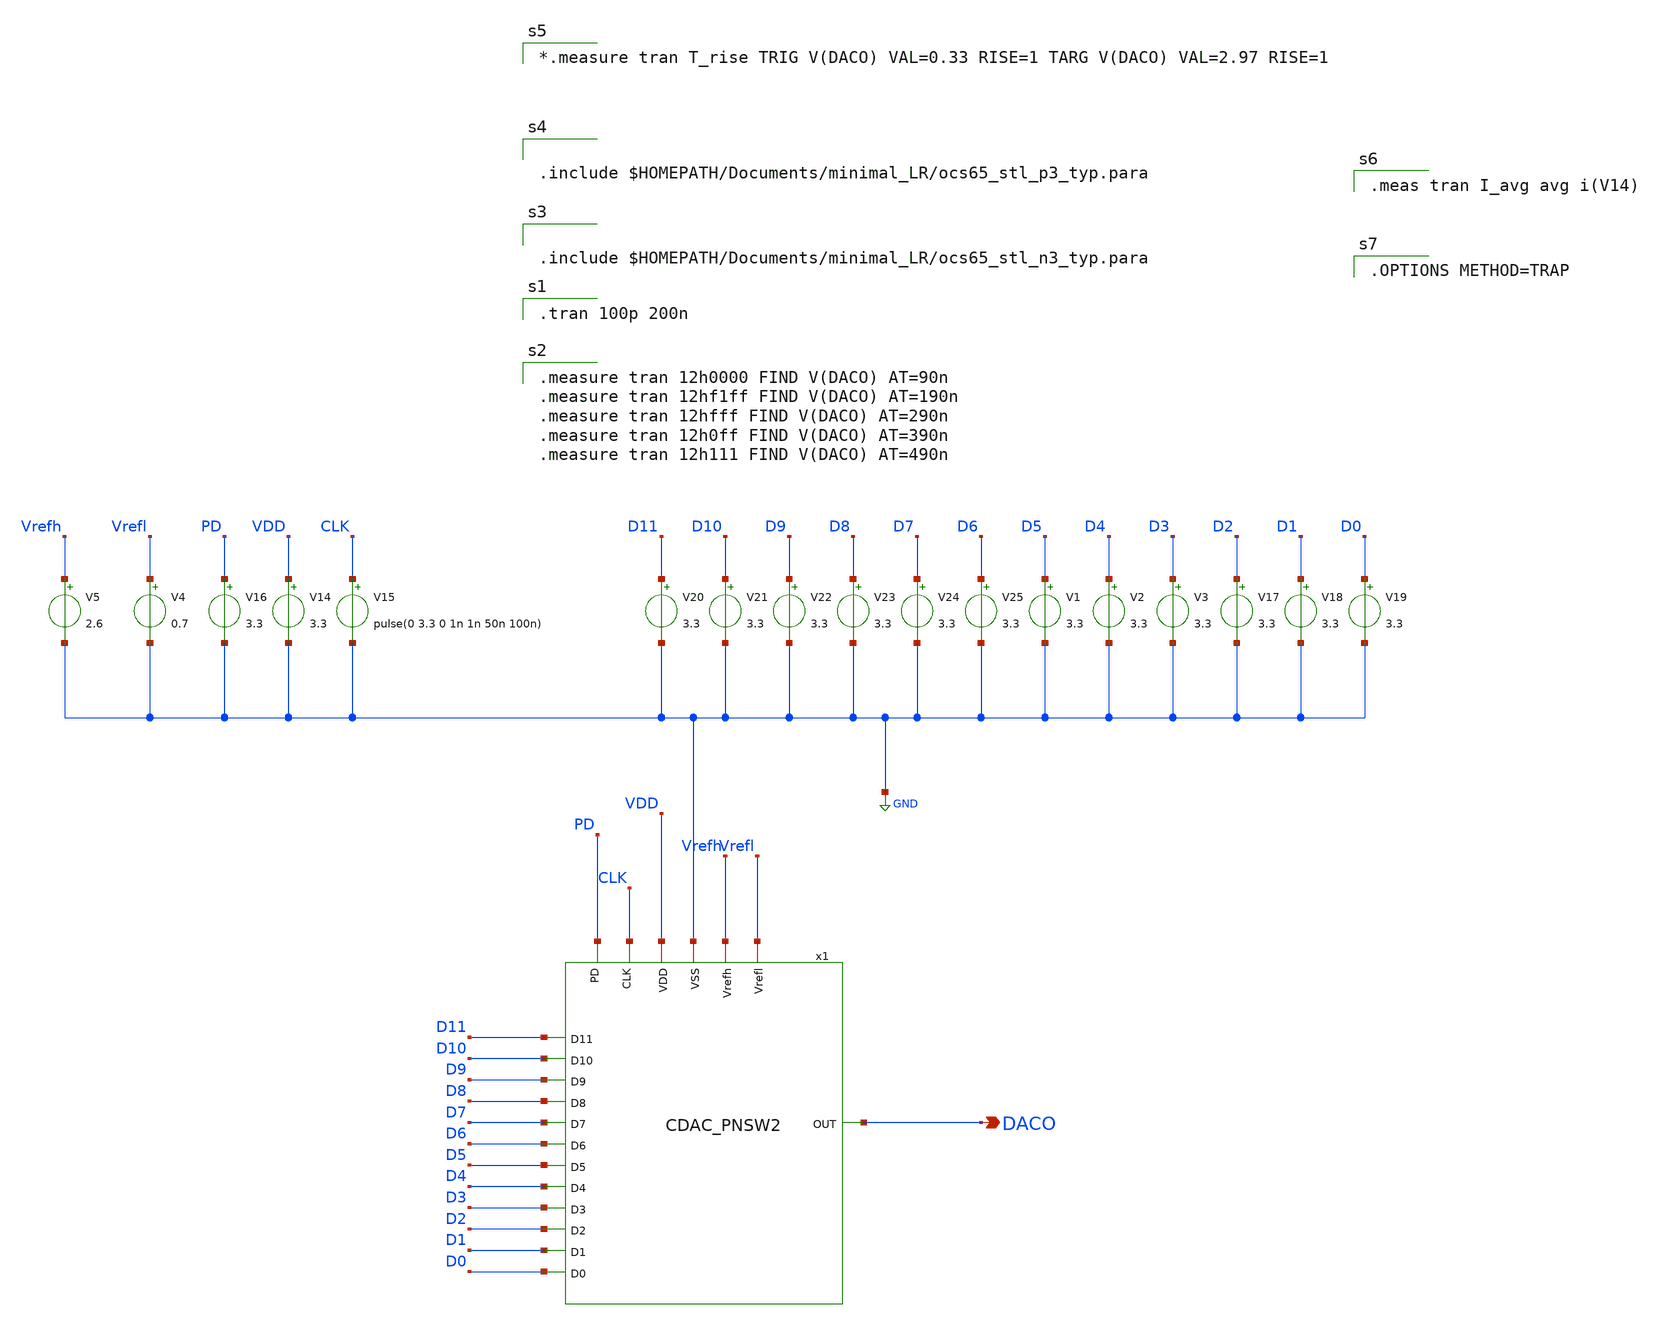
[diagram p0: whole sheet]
** sch_path: CDAC_sim.sch
**.subckt CDAC_sim DACO
*.opin DACO
V14 VDD GND 3.3
V15 CLK GND pulse(0 3.3 0 1n 1n 50n 100n)
V16 PD GND 3.3
V1 D5 GND 3.3
V2 D4 GND 3.3
V3 D3 GND 3.3
V17 D2 GND 3.3
V18 D1 GND 3.3
V19 D0 GND 3.3
V20 D11 GND 3.3
V21 D10 GND 3.3
V22 D9 GND 3.3
V23 D8 GND 3.3
V24 D7 GND 3.3
V25 D6 GND 3.3
V4 Vrefl GND 0.7
V5 Vrefh GND 2.6
x1 CLK D11 D7 D10 D1 D0 D9 D8 D2 D6 D5 D4 D3 DACO GND VDD Vrefl Vrefh PD CDAC_PNSW2
**** begin user architecture code

.tran 100p 200n


.measure tran 12h0000 FIND V(DACO) AT=90n
.measure tran 12hf1ff FIND V(DACO) AT=190n
.measure tran 12hfff FIND V(DACO) AT=290n
.measure tran 12h0ff FIND V(DACO) AT=390n
.measure tran 12h111 FIND V(DACO) AT=490n



.include $HOMEPATH/Documents/minimal_LR/ocs65_stl_n3_typ.para



.include $HOMEPATH/Documents/minimal_LR/ocs65_stl_p3_typ.para


*.measure tran T_rise TRIG V(DACO) VAL=0.33 RISE=1 TARG V(DACO) VAL=2.97 RISE=1


.meas tran I_avg avg i(V14)


.OPTIONS METHOD=TRAP

**** end user architecture code
**.ends

* expanding   symbol:  CDAC_PNSW2.sym # of pins=19
** sym_path: CDAC_PNSW2.sym
** sch_path: CDAC_PNSW2.sch
.subckt CDAC_PNSW2 CLK D11 D7 D10 D1 D0 D9 D8 D2 D6 D5 D4 D3 OUT VSS VDD Vrefl Vrefh PD
*.opin OUT
*.iopin Vrefh
*.iopin Vrefl
*.ipin D11
*.ipin D10
*.ipin D9
*.ipin D8
*.ipin D7
*.ipin D6
*.ipin D5
*.ipin D4
*.ipin D3
*.ipin D2
*.ipin D1
*.ipin D0
*.ipin CLK
*.ipin PD
*.iopin VDD
*.iopin VSS
C1 OUT net1 33f m=1
x17 VDD D11b D11 VSS INV
x18 VDD D10b D10 VSS INV
x34 VDD D9b D9 VSS INV
x35 VDD D8b D8 VSS INV
x36 VDD D7b D7 VSS INV
x37 VDD D6b D6 VSS INV
x38 VDD D5b D5 VSS INV
x39 VDD D4b D4 VSS INV
x40 VDD D3b D3 VSS INV
x41 VDD D2b D2 VSS INV
x42 VDD D1b D1 VSS INV
x43 VDD D0b D0 VSS INV
x72 VDD CLK CLK1 VSS net2 NOL
x73 VDD CLK2 net2 VSS INV
x74 VDD net3 PD VSS INV
x75 VDD net4 resetPD net3 VSS OR
x46 VDD D11A CLK1 D11b VSS IMPLY
x47 VDD D10A CLK1 D10b VSS IMPLY
x48 VDD D9A CLK1 D9b VSS IMPLY
x49 VDD D8A CLK1 D8b VSS IMPLY
x50 VDD D7A CLK1 D7b VSS IMPLY
x51 VDD D6A CLK1 D6b VSS IMPLY
x52 VDD D5A CLK1 D5b VSS IMPLY
x53 VDD D4A CLK1 D4b VSS IMPLY
x54 VDD D3A CLK1 D3b VSS IMPLY
x55 VDD D2A CLK1 D2b VSS IMPLY
x56 VDD D1A CLK1 D1b VSS IMPLY
x57 VDD D0A CLK1 D0b VSS IMPLY
x58 VDD D0bO CLK2 D0b VSS IMPLY
x59 VDD D1bO CLK2 D1b VSS IMPLY
x60 VDD D2bO CLK2 D2b VSS IMPLY
x61 VDD D3bO CLK2 D3b VSS IMPLY
x62 VDD D4bO CLK2 D4b VSS IMPLY
x63 VDD D5bO CLK2 D5b VSS IMPLY
x64 VDD D6bO CLK2 D6b VSS IMPLY
x65 VDD D7bO CLK2 D7b VSS IMPLY
x66 VDD D8bO CLK2 D8b VSS IMPLY
x67 VDD D9bO CLK2 D9b VSS IMPLY
x68 VDD D10bO CLK2 D10b VSS IMPLY
x69 VDD D11bO CLK2 D11b VSS IMPLY
x76 VDD net4 CLK2 VSS INV
M1 OUT resetPD Vrefl VSS nch w=5u l=0.35u as=0 ps=0 ad=0 pd=0 m=20
C2 OUT net5 33f m=1
C3 OUT net16 33f m=2
C4 OUT net15 33f m=4
C5 OUT net14 33f m=8
C6 OUT net13 33f m=16
C7 OUT net12 33f m=32
C8 OUT net11 33f m=64
C9 OUT net10 33f m=128
C10 OUT net9 33f m=256
C11 OUT net8 33f m=512
C12 OUT net7 33f m=1024
C13 OUT net6 33f m=2048
M2 net5 D0bO Vrefl VSS nch w=0.7u l=0.35u as=0 ps=0 ad=0 pd=0 m=1
M5 Vrefh D0A net5 VDD pch w=0.7u l=0.35u as=0 ps=0 ad=0 pd=0 m=1
M3 net16 D1bO Vrefl VSS nch w=0.7u l=0.35u as=0 ps=0 ad=0 pd=0 m=2
M4 Vrefh D1A net16 VDD pch w=0.7u l=0.35u as=0 ps=0 ad=0 pd=0 m=2
M6 net15 D2bO Vrefl VSS nch w=0.7u l=0.35u as=0 ps=0 ad=0 pd=0 m=4
M7 Vrefh D2A net15 VDD pch w=0.7u l=0.35u as=0 ps=0 ad=0 pd=0 m=4
M8 net14 D3bO Vrefl VSS nch w=0.7u l=0.35u as=0 ps=0 ad=0 pd=0 m=8
M9 Vrefh D3A net14 VDD pch w=0.7u l=0.35u as=0 ps=0 ad=0 pd=0 m=8
M10 net13 D4bO Vrefl VSS nch w=0.7u l=0.35u as=0 ps=0 ad=0 pd=0 m=16
M11 Vrefh D4A net13 VDD pch w=0.7u l=0.35u as=0 ps=0 ad=0 pd=0 m=16
M12 net12 D5bO Vrefl VSS nch w=0.7u l=0.35u as=0 ps=0 ad=0 pd=0 m=32
M13 Vrefh D5A net12 VDD pch w=0.7u l=0.35u as=0 ps=0 ad=0 pd=0 m=32
M14 net11 D6bO Vrefl VSS nch w=0.7u l=0.35u as=0 ps=0 ad=0 pd=0 m=64
M15 Vrefh D6A net11 VDD pch w=0.7u l=0.35u as=0 ps=0 ad=0 pd=0 m=64
M16 net10 D7bO Vrefl VSS nch w=0.7u l=0.35u as=0 ps=0 ad=0 pd=0 m=128
M17 Vrefh D7A net10 VDD pch w=0.7u l=0.35u as=0 ps=0 ad=0 pd=0 m=128
M18 net9 D8bO Vrefl VSS nch w=0.7u l=0.35u as=0 ps=0 ad=0 pd=0 m=256
M19 Vrefh D8A net9 VDD pch w=0.7u l=0.35u as=0 ps=0 ad=0 pd=0 m=256
M20 net8 D9bO Vrefl VSS nch w=0.7u l=0.35u as=0 ps=0 ad=0 pd=0 m=512
M21 Vrefh D9A net8 VDD pch w=0.7u l=0.35u as=0 ps=0 ad=0 pd=0 m=512
M22 net7 D10bO Vrefl VSS nch w=0.7u l=0.35u as=0 ps=0 ad=0 pd=0 m=1024
M23 Vrefh D10A net7 VDD pch w=0.7u l=0.35u as=0 ps=0 ad=0 pd=0 m=1024
M24 net6 D11bO Vrefl VSS nch w=0.7u l=0.35u as=0 ps=0 ad=0 pd=0 m=2048
M25 Vrefh D11A net6 VDD pch w=0.7u l=0.35u as=0 ps=0 ad=0 pd=0 m=2048
M26 net1 VDD Vrefl VSS nch w=0.7u l=0.35u as=0 ps=0 ad=0 pd=0 m=1
.ends


* expanding   symbol:  INV.sym # of pins=4
** sym_path: INV.sym
** sch_path: INV.sch
.subckt INV VDD OUT IN VSS
*.opin OUT
*.ipin IN
*.iopin VDD
*.iopin VSS
M2 OUT IN VDD VDD pch w=10u l=0.35u as=0 ps=0 ad=0 pd=0 m=1
M1 OUT IN VSS VSS nch w=5u l=0.35u as=0 ps=0 ad=0 pd=0 m=1
.ends


* expanding   symbol:  NOL.sym # of pins=5
** sym_path: NOL.sym
** sch_path: NOL.sch
.subckt NOL VDD CLK CLK1 VSS CLK2
*.ipin CLK
*.opin CLK1
*.opin CLK2
*.iopin VDD
*.iopin VSS
x3 VDD net1 CLK VSS INV
x1 VDD CLK net9 CLK2 VSS NOR
x2 VDD CLK1 net2 net1 VSS NOR
x4 VDD net3 net2 VSS INV
x5 VDD net4 net3 VSS INV
x6 VDD net5 net4 VSS INV
x7 VDD net17 net5 VSS INV
x8 VDD net6 net9 VSS INV
x9 VDD net7 net6 VSS INV
x10 VDD net8 net7 VSS INV
x11 VDD net13 net8 VSS INV
x12 VDD net10 net13 VSS INV
x13 VDD net11 net10 VSS INV
x14 VDD net12 net11 VSS INV
x15 VDD net32 net12 VSS INV
x16 VDD net14 net17 VSS INV
x17 VDD net15 net14 VSS INV
x18 VDD net16 net15 VSS INV
x19 VDD net33 net16 VSS INV
x20 VDD net18 net33 VSS INV
x21 VDD net19 net18 VSS INV
x22 VDD net20 net19 VSS INV
x23 VDD net24 net20 VSS INV
x24 VDD net21 net24 VSS INV
x25 VDD net22 net21 VSS INV
x26 VDD net23 net22 VSS INV
x27 VDD net34 net23 VSS INV
x28 VDD net25 net32 VSS INV
x29 VDD net26 net25 VSS INV
x30 VDD net27 net26 VSS INV
x31 VDD net31 net27 VSS INV
x32 VDD net28 net31 VSS INV
x33 VDD net29 net28 VSS INV
x34 VDD net30 net29 VSS INV
x35 VDD net50 net30 VSS INV
x36 VDD net35 net34 VSS INV
x37 VDD net36 net35 VSS INV
x38 VDD net37 net36 VSS INV
x39 VDD net41 net37 VSS INV
x40 VDD net38 net41 VSS INV
x41 VDD net39 net38 VSS INV
x42 VDD net40 net39 VSS INV
x43 VDD net42 net40 VSS INV
x44 VDD net43 net50 VSS INV
x45 VDD net44 net43 VSS INV
x46 VDD net45 net44 VSS INV
x47 VDD net49 net45 VSS INV
x48 VDD net46 net49 VSS INV
x49 VDD net47 net46 VSS INV
x50 VDD net48 net47 VSS INV
x51 VDD net61 net48 VSS INV
x52 VDD net51 net42 VSS INV
x53 VDD net53 net51 VSS INV
x54 VDD net52 net61 VSS INV
x55 VDD net60 net52 VSS INV
x56 VDD net54 net53 VSS INV
x57 VDD net55 net54 VSS INV
x58 VDD net56 net55 VSS INV
x59 VDD CLK2 net56 VSS INV
x64 VDD net57 net60 VSS INV
x65 VDD net58 net57 VSS INV
x66 VDD net59 net58 VSS INV
x67 VDD CLK1 net59 VSS INV
.ends


* expanding   symbol:  OR.sym # of pins=5
** sym_path: OR.sym
** sch_path: OR.sch
.subckt OR VDD A Y B VSS
*.iopin VDD
*.ipin A
*.ipin B
*.iopin VSS
*.opin Y
M1 net1 A VSS VSS nch w=3.5u l=0.35u as=0 ps=0 ad=0 pd=0 m=1
M2 net2 A VDD VDD pch w=3.5u l=0.35u as=0 ps=0 ad=0 pd=0 m=1
M3 net1 B net2 VDD pch w=3.5u l=0.35u as=0 ps=0 ad=0 pd=0 m=1
M4 net1 B VSS VSS nch w=3.5u l=0.35u as=0 ps=0 ad=0 pd=0 m=1
M5 Y net1 VDD VDD pch w=3.5u l=0.35u as=0 ps=0 ad=0 pd=0 m=1
M6 Y net1 VSS VSS nch w=3.5u l=0.35u as=0 ps=0 ad=0 pd=0 m=1
.ends


* expanding   symbol:  IMPLY.sym # of pins=5
** sym_path: IMPLY.sym
** sch_path: IMPLY.sch
.subckt IMPLY VDD Y A B VSS
*.ipin A
*.ipin B
*.iopin VDD
*.iopin VSS
*.opin Y
x2 VDD net1 A VSS INV
x1 VDD net1 Y B VSS OR
.ends


* expanding   symbol:  NOR.sym # of pins=5
** sym_path: NOR.sym
** sch_path: NOR.sch
.subckt NOR VDD A Y B VSS
*.iopin VDD
*.ipin A
*.ipin B
*.iopin VSS
*.opin Y
M1 Y A VSS VSS nch w=3.5u l=0.35u as=0 ps=0 ad=0 pd=0 m=1
M2 net1 A VDD VDD pch w=3.5u l=0.35u as=0 ps=0 ad=0 pd=0 m=1
M3 Y B net1 VDD pch w=3.5u l=0.35u as=0 ps=0 ad=0 pd=0 m=1
M4 Y B VSS VSS nch w=3.5u l=0.35u as=0 ps=0 ad=0 pd=0 m=1
.ends

.GLOBAL GND
.end
